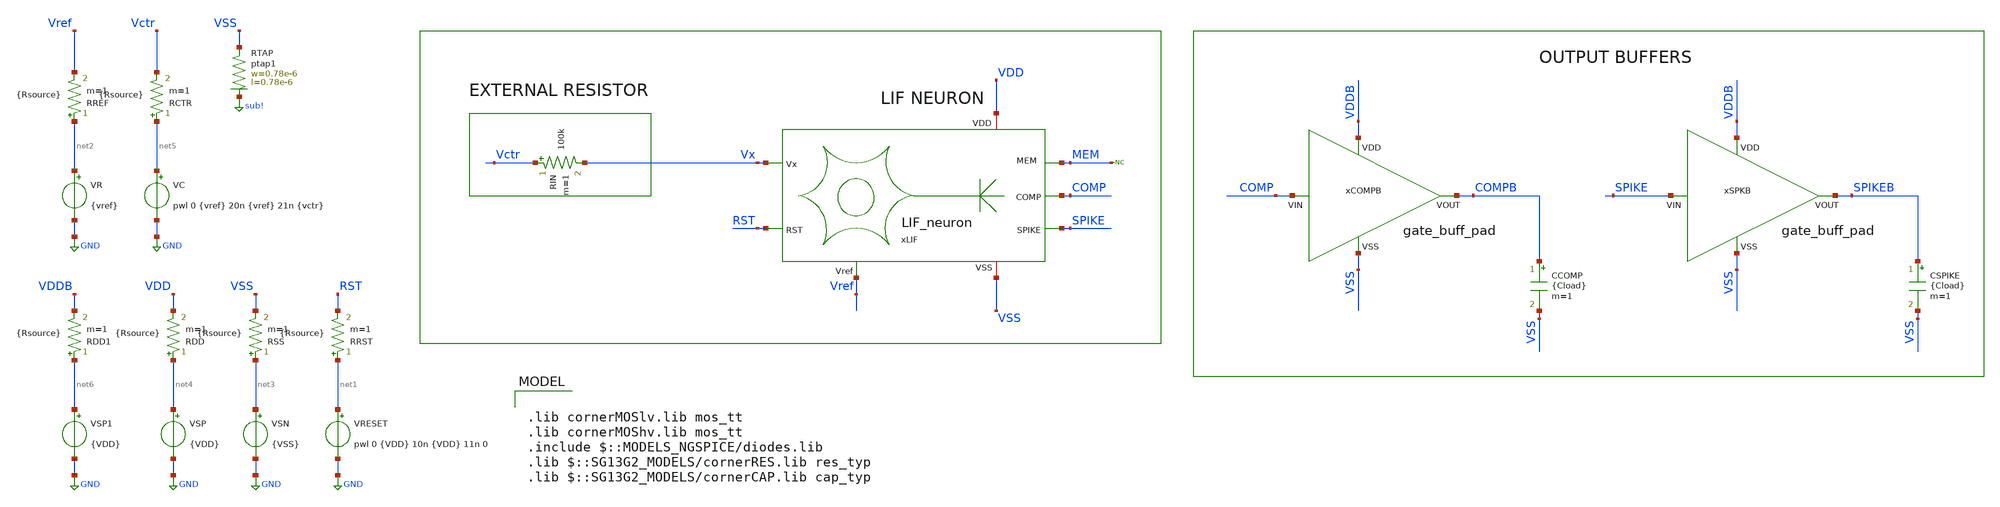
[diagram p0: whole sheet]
** sch_path: work/LIF_neuron/xschem/LIF_Neuron_tb_current.sch
**.subckt LIF_Neuron_tb_current
VRESET net1 GND pwl 0 {VDD} 10n {VDD} 11n 0
VSN net3 GND {VSS}
VR net2 GND {vref}
VC net5 GND pwl 0 {vref} 20n {vref} 21n {vctr}
xLIF VDD Vx MEM RST SPIKE VSS Vref COMP LIF_neuron
RDD net4 VDD {Rsource} m=1
RSS net3 VSS {Rsource} m=1
RRST net1 RST {Rsource} m=1
RREF net2 Vref {Rsource} m=1
RCTR net5 Vctr {Rsource} m=1
CSPIKE SPIKEB VSS {Cload} m=1
RIN Vctr Vx 100k m=1
VSP net4 GND {VDD}
* noconn MEM
XRTAP VSS sub! ptap1 R=262.8 w=0.78e-6 l=0.78e-6
xSPKB VDDB SPIKE SPIKEB VSS gate_buff_pad
xCOMPB VDDB COMP COMPB VSS gate_buff_pad
RDD1 net6 VDDB {Rsource} m=1
VSP1 net6 GND {VDD}
CCOMP COMPB VSS {Cload} m=1
**** begin user architecture code



.param VDD = 0.6
.param VSS = 0
.param vctr = 0
.param vref = 0.6
.param Cload = 20p
.param Rsource = 1m

.param sw_stat_global = 0
.param sw_stat_mismatch = 0

.save @v.xLIF.VINT[i]
.save @v.xLIF.VCOMP[i]
.save @v.xLIF.VSPIKE[i]

.save all

.control

* >> Variables <<
let Vhigh = 0.5
let Vmid = Vhigh * 0.5
let tstop = 0.1u
let tstep = tstop/10k

* Run transient analysis
tran $&tstep $&tstop

* Average current
let IDD = -1*i(VSP)
let i_VINT = @v.xLIF.VINT[i]
let i_VCOMP = @v.xLIF.VCOMP[i]
let i_VSPIKE = @v.xLIF.VSPIKE[i]

*meas tran i_VINT AVG i_VINT from=11n to=tstop
*meas tran i_VCOMP AVG i_VCOMP from=11n to=tstop
*meas tran i_VSPIKE AVG i_VSPIKE from=11n to=tstop
meas tran I_avg AVG IDD from=11n to=tstop
let P_avg = abs(I_avg*Vhigh)

meas TRAN T_spk TRIG v(SPIKE) VAL=Vmid rise=2 TARG v(SPIKE) VAL=Vmid rise=3
let F_spk = 1 / T_spk
let E_spk = P_avg/F_spk

*Print Neuron results
print F_spk I_avg P_avg E_spk

*Print internal currents
*print i_VINT i_VCOMP i_VSPIKE

* Plots
plot v(Vctr) v(Vref) v(RST)
plot v(MEM) v(Vx) v(vctr)
plot v(COMP) v(SPIKE)
plot v(COMPB) v(SPIKEB)

.endc



.lib cornerMOSlv.lib mos_tt
.lib cornerMOShv.lib mos_tt
.include $::MODELS_NGSPICE/diodes.lib
.lib $::SG13G2_MODELS/cornerRES.lib res_typ
.lib $::SG13G2_MODELS/cornerCAP.lib cap_typ

**** end user architecture code
**.ends
.GLOBAL GND
.GLOBAL sub!
.end
